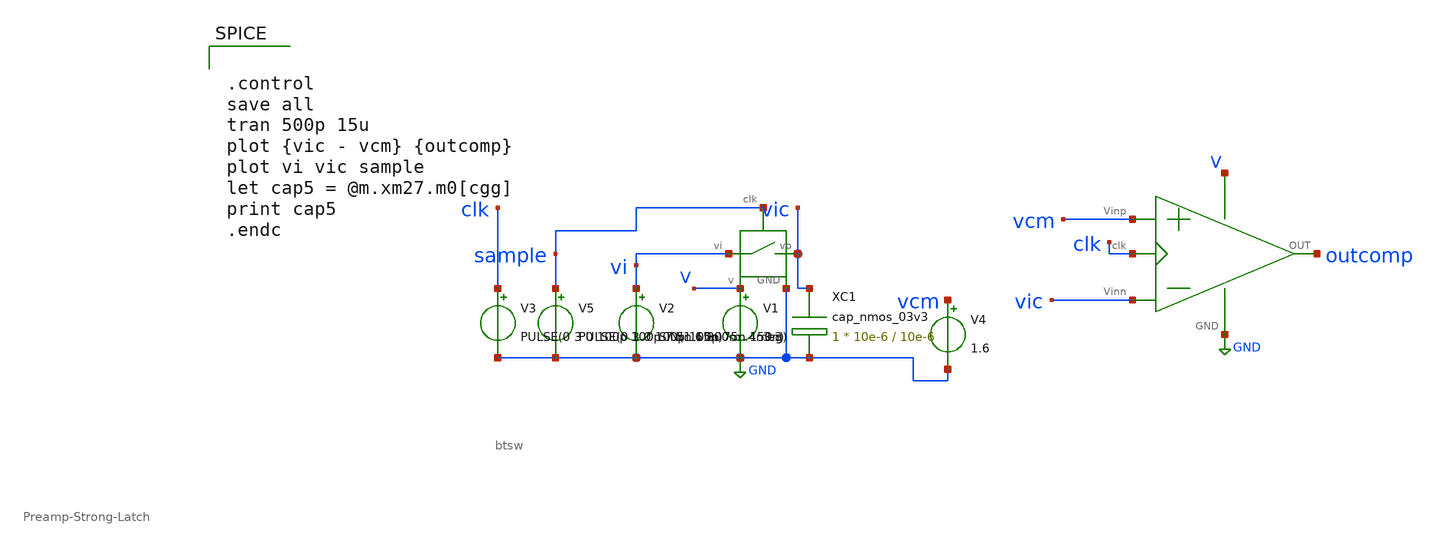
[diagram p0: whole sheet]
** sch_path: btsw/btsw_2.sch
**.subckt btsw_2
V1 V GND 3.3
V2 vi GND SIN(1.6 800m .4meg)
V3 clk GND PULSE(0 3 0 100p 100p 7.5n 15n)
X1 sample vi vic V GND btsw
V4 vcm GND 1.6
V5 sample GND PULSE(0 3 0 100p 100p 75n 150n)
XC1 vic GND cap_nmos_03v3 c_width=10e-6 c_length=10e-6 m=1
X1 V GND vcm vic outcomp clk Preamp-Strong-Latch
**** begin user architecture code


.control
save all
tran 500p 15u
plot {vic - vcm} {outcomp}
plot vi vic sample
let cap5 = @m.xm27.m0[cgg]
print cap5
.endc


.include /foss/pdks/gf180mcuC/libs.tech/ngspice/design.ngspice
.lib /foss/pdks/gf180mcuC/libs.tech/ngspice/sm141064.ngspice typical
.lib /foss/pdks/gf180mcuC/libs.tech/ngspice/sm141064.ngspice moscap_typical

**** end user architecture code
**.ends
.GLOBAL GND
.end
